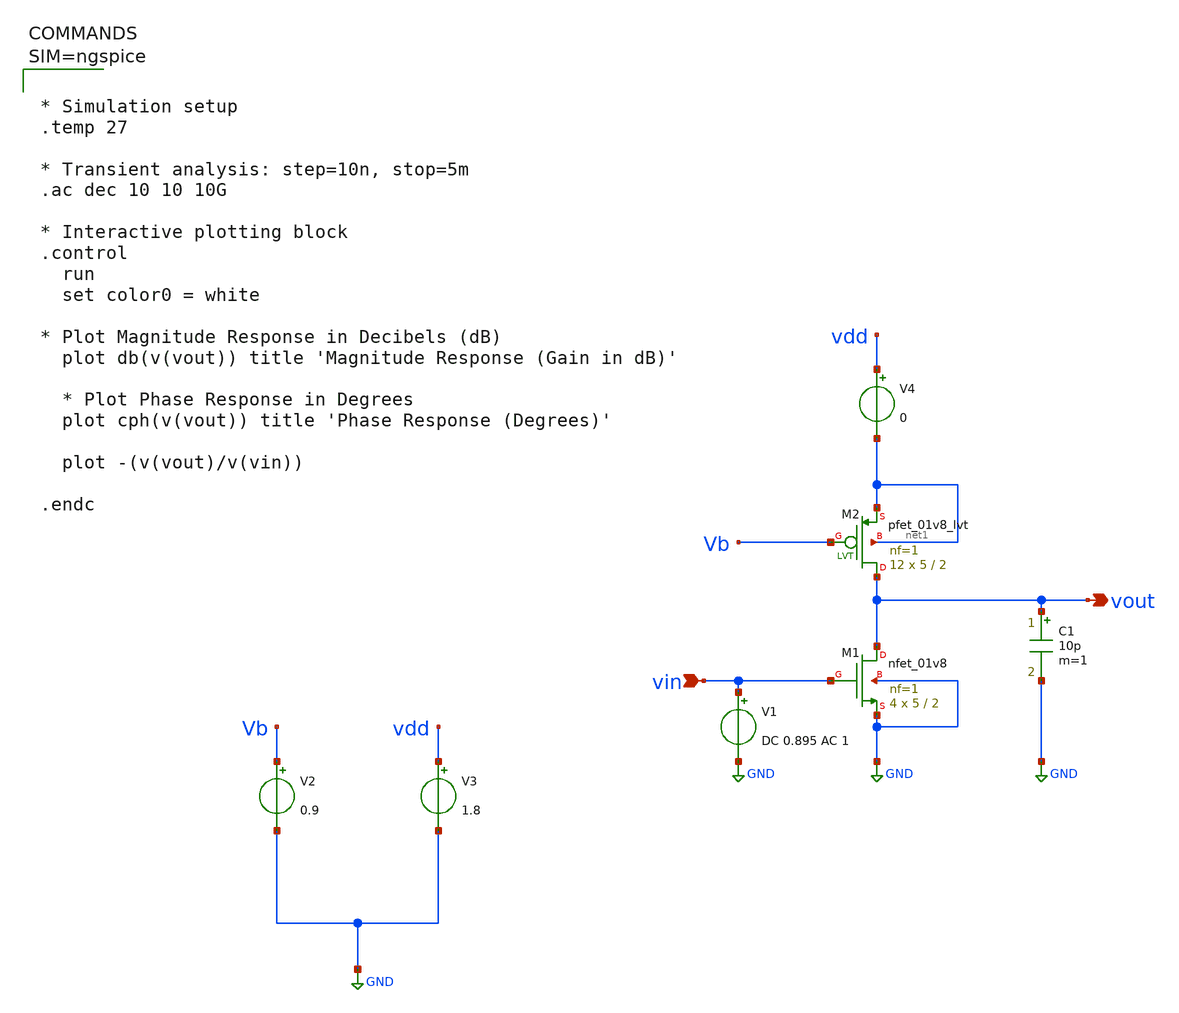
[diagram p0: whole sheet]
** sch_path: testbenches/NMOS_pmos_load_DB.sch
**.subckt NMOS_pmos_load_DB vin vout
*.ipin vin
*.opin vout
C1 vout GND 10p m=1
V1 vin GND DC 0.895 AC 1
V2 Vb GND 0.9
V3 vdd GND 1.8
XM2 vout Vb net1 net1 sky130_fd_pr__pfet_01v8_lvt L=2 W=5 nf=1 ad='int((1 + 1)/2) * 5 / 1 * 0.29' as='int((1 + 2)/2) * 5 / 1 * 0.29'
+ pd='2*int((1 + 1)/2) * (5 / 1 + 0.29)' ps='2*int((1 + 2)/2) * (5 / 1 + 0.29)' nrd='0.29 / 5 ' nrs='0.29 / 5 '
+ sa=0 sb=0 sd=0 mult=12 m=12
XM1 vout vin GND GND sky130_fd_pr__nfet_01v8 L=2 W=5 nf=1 ad='int((1 + 1)/2) * 5 / 1 * 0.29' as='int((1 + 2)/2) * 5 / 1 * 0.29'
+ pd='2*int((1 + 1)/2) * (5 / 1 + 0.29)' ps='2*int((1 + 2)/2) * (5 / 1 + 0.29)' nrd='0.29 / 5 ' nrs='0.29 / 5 '
+ sa=0 sb=0 sd=0 mult=4 m=4
V4 vdd net1 0
**** begin user architecture code

** opencircuitdesign pdks install
.lib $::SKYWATER_MODELS/sky130.lib.spice tt




* Simulation setup
.temp 27

* Transient analysis: step=10n, stop=5m
.ac dec 10 10 10G

* Interactive plotting block
.control
  run
  set color0 = white

* Plot Magnitude Response in Decibels (dB)
  plot db(v(vout)) title 'Magnitude Response (Gain in dB)'

  * Plot Phase Response in Degrees
  plot cph(v(vout)) title 'Phase Response (Degrees)'

  plot -(v(vout)/v(vin))

.endc




**** end user architecture code
**.ends
.GLOBAL GND
.end
